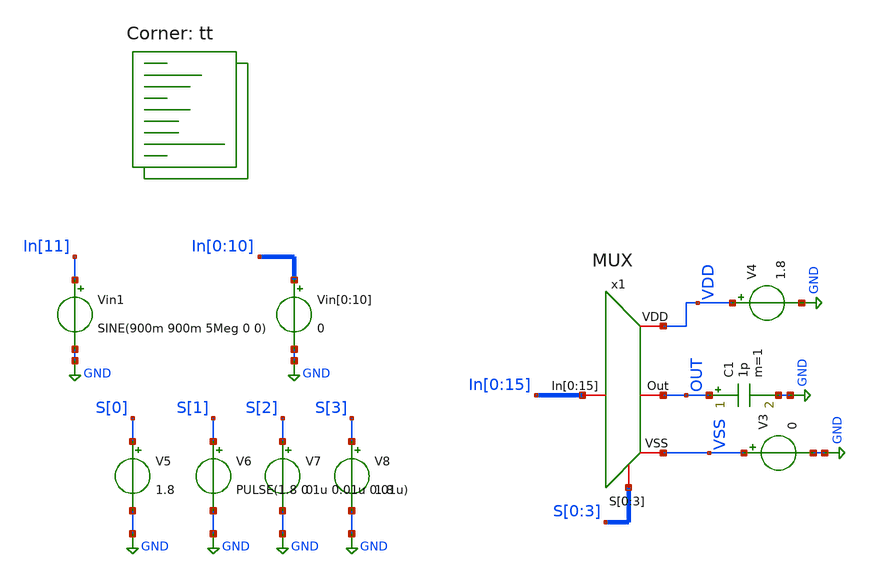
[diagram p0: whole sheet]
** sch_path: MUX/TB_MUX.sch
**.subckt TB_MUX
x1 VDD VSS In[0] In[1] In[2] In[3] In[4] In[5] In[6] In[7] In[8] In[9] In[10] In[11] In[12] In[13]
+ In[14] In[15] OUT S[0] S[1] S[2] S[3] MUX
Vin1 In[11] GND SINE(900m 900m 5Meg 0 0)
V4 VDD GND 1.8
V5 S[0] GND 1.8
V6 S[1] GND PULSE(1.8 0 1u 0.01u 0.01u)
V7 S[2] GND 0
V8 S[3] GND 1.8
V3 VSS GND 0
C1 OUT GND 1p m=1
Vin[0] In[0] GND 0
Vin[1] In[1] GND 0
Vin[2] In[2] GND 0
Vin[3] In[3] GND 0
Vin[4] In[4] GND 0
Vin[5] In[5] GND 0
Vin[6] In[6] GND 0
Vin[7] In[7] GND 0
Vin[8] In[8] GND 0
Vin[9] In[9] GND 0
Vin[10] In[10] GND 0
**** begin user architecture code


.tran 0.001u 2u
.save all


.lib $::SKYWATER_MODELS/sky130.lib.spice tt
**** end user architecture code
**.ends

* expanding   symbol:  MUX.sym # of pins=5
** sym_path: MUX/MUX.sym
** sch_path: MUX/MUX.sch
.subckt MUX VDD VSS In[0] In[1] In[2] In[3] In[4] In[5] In[6] In[7] In[8] In[9] In[10] In[11] In[12]
+ In[13] In[14] In[15] Out S[0] S[1] S[2] S[3]
*.iopin VDD
*.iopin VSS
*.iopin
*+ In[0],In[1],In[2],In[3],In[4],In[5],In[6],In[7],In[8],In[9],In[10],In[11],In[12],In[13],In[14],In[15]
*.iopin Out
*.iopin S[0],S[1],S[2],S[3]
X[0] S[0] VDD R0[0] In[0] VSS S[0]B MUX_TG
x1 VDD S[0]B S[0] VSS inverter
X[13] S[1] VDD R1[0] R0[0] VSS S[1]B MUX_TG
x2 VDD S[1]B S[1] VSS inverter
X[19] S[2] VDD R2[0] R1[0] VSS S[2]B MUX_TG
x3 VDD S[2]B S[2] VSS inverter
x4 VDD S[3]B S[3] VSS inverter
X[22] S[3] VDD Out R2[0] VSS S[3]B MUX_TG
X[1] S[0]B VDD R0[0] In[1] VSS S[0] MUX_TG
X[14] S[1]B VDD R1[0] R0[1] VSS S[1] MUX_TG
X[20] S[2]B VDD R2[0] R1[1] VSS S[2] MUX_TG
X[23] S[3]B VDD Out R2[1] VSS S[3] MUX_TG
X[2] S[0] VDD R0[1] In[2] VSS S[0]B MUX_TG
X[15] S[1] VDD R1[1] R0[2] VSS S[1]B MUX_TG
X[21] S[2] VDD R2[1] R1[2] VSS S[2]B MUX_TG
X[3] S[0]B VDD R0[1] In[3] VSS S[0] MUX_TG
X[16] S[1]B VDD R1[1] R0[3] VSS S[1] MUX_TG
X[4] S[0] VDD R0[2] In[4] VSS S[0]B MUX_TG
X[17] S[1] VDD R1[2] R0[4] VSS S[1]B MUX_TG
X[5] S[0]B VDD R0[2] In[5] VSS S[0] MUX_TG
X[18] S[1]B VDD R1[2] R0[5] VSS S[1] MUX_TG
X[6] S[0] VDD R0[3] In[6] VSS S[0]B MUX_TG
X[7] S[0]B VDD R0[3] In[7] VSS S[0] MUX_TG
X[8] S[0] VDD R0[4] In[8] VSS S[0]B MUX_TG
X[9] S[0]B VDD R0[4] In[9] VSS S[0] MUX_TG
X[10] S[0] VDD R0[5] In[10] VSS S[0]B MUX_TG
X[11] S[0]B VDD R0[5] In[11] VSS S[0] MUX_TG
.ends


* expanding   symbol:  MUX_TG.sym # of pins=6
** sym_path: MUX/MUX_TG.sym
** sch_path: MUX/MUX_TG.sch
.subckt MUX_TG AB VDD Out In VSS A
*.iopin In
*.iopin Out
*.iopin VDD
*.iopin VSS
*.iopin AB
*.iopin A
XM1 In A Out VSS sky130_fd_pr__nfet_01v8 L=0.15 W=2.1 nf=1 ad='int((nf+1)/2) * W/nf * 0.29' as='int((nf+2)/2) * W/nf * 0.29'
+ pd='2*int((nf+1)/2) * (W/nf + 0.29)' ps='2*int((nf+2)/2) * (W/nf + 0.29)' nrd='0.29 / W' nrs='0.29 / W'
+ sa=0 sb=0 sd=0 mult=2 m=2
XM2 In AB Out VDD sky130_fd_pr__pfet_01v8 L=0.15 W=4.75 nf=1 ad='int((nf+1)/2) * W/nf * 0.29' as='int((nf+2)/2) * W/nf * 0.29'
+ pd='2*int((nf+1)/2) * (W/nf + 0.29)' ps='2*int((nf+2)/2) * (W/nf + 0.29)' nrd='0.29 / W' nrs='0.29 / W'
+ sa=0 sb=0 sd=0 mult=4 m=4
.ends


* expanding   symbol:  inverter.sym # of pins=4
** sym_path: MUX/inverter.sym
** sch_path: MUX/inverter.sch
.subckt inverter VDD Out In VSS
*.iopin VDD
*.iopin Out
*.iopin VSS
*.iopin In
XM3 Out In VSS VSS sky130_fd_pr__nfet_01v8 L=0.15 W=2.1 nf=1 ad='int((nf+1)/2) * W/nf * 0.29' as='int((nf+2)/2) * W/nf * 0.29'
+ pd='2*int((nf+1)/2) * (W/nf + 0.29)' ps='2*int((nf+2)/2) * (W/nf + 0.29)' nrd='0.29 / W' nrs='0.29 / W'
+ sa=0 sb=0 sd=0 mult=2 m=2
XM1 Out In VDD VDD sky130_fd_pr__pfet_01v8 L=0.15 W=4.75 nf=1 ad='int((nf+1)/2) * W/nf * 0.29' as='int((nf+2)/2) * W/nf * 0.29'
+ pd='2*int((nf+1)/2) * (W/nf + 0.29)' ps='2*int((nf+2)/2) * (W/nf + 0.29)' nrd='0.29 / W' nrs='0.29 / W'
+ sa=0 sb=0 sd=0 mult=4 m=4
.ends

.GLOBAL GND
.end
